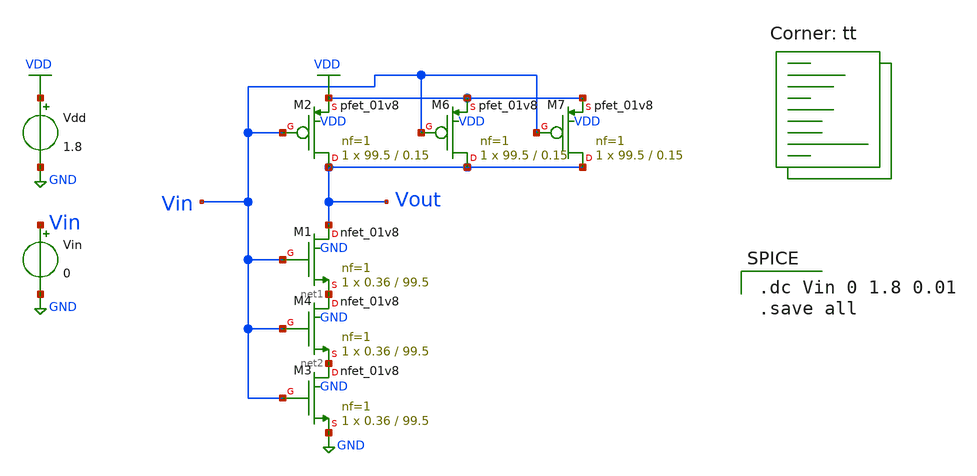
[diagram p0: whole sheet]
** sch_path: vdd1.8V/inverter_sat_16.sch
**.subckt inverter_sat_16
Vdd VDD GND 1.8
XM1 Vout Vin net1 GND sky130_fd_pr__nfet_01v8 L=99.5 W=0.36 nf=1 ad='int((nf+1)/2) * W/nf * 0.29' as='int((nf+2)/2) * W/nf * 0.29'
+ pd='2*int((nf+1)/2) * (W/nf + 0.29)' ps='2*int((nf+2)/2) * (W/nf + 0.29)' nrd='0.29 / W' nrs='0.29 / W'
+ sa=0 sb=0 sd=0 mult=1 m=1
XM2 Vout Vin VDD VDD sky130_fd_pr__pfet_01v8 L=0.15 W=99.5 nf=1 ad='int((nf+1)/2) * W/nf * 0.29' as='int((nf+2)/2) * W/nf * 0.29'
+ pd='2*int((nf+1)/2) * (W/nf + 0.29)' ps='2*int((nf+2)/2) * (W/nf + 0.29)' nrd='0.29 / W' nrs='0.29 / W'
+ sa=0 sb=0 sd=0 mult=1 m=1
Vin Vin GND 0
XM6 Vout Vin VDD VDD sky130_fd_pr__pfet_01v8 L=0.15 W=99.5 nf=1 ad='int((nf+1)/2) * W/nf * 0.29' as='int((nf+2)/2) * W/nf * 0.29'
+ pd='2*int((nf+1)/2) * (W/nf + 0.29)' ps='2*int((nf+2)/2) * (W/nf + 0.29)' nrd='0.29 / W' nrs='0.29 / W'
+ sa=0 sb=0 sd=0 mult=1 m=1
XM7 Vout Vin VDD VDD sky130_fd_pr__pfet_01v8 L=0.15 W=99.5 nf=1 ad='int((nf+1)/2) * W/nf * 0.29' as='int((nf+2)/2) * W/nf * 0.29'
+ pd='2*int((nf+1)/2) * (W/nf + 0.29)' ps='2*int((nf+2)/2) * (W/nf + 0.29)' nrd='0.29 / W' nrs='0.29 / W'
+ sa=0 sb=0 sd=0 mult=1 m=1
XM4 net1 Vin net2 GND sky130_fd_pr__nfet_01v8 L=99.5 W=0.36 nf=1 ad='int((nf+1)/2) * W/nf * 0.29' as='int((nf+2)/2) * W/nf * 0.29'
+ pd='2*int((nf+1)/2) * (W/nf + 0.29)' ps='2*int((nf+2)/2) * (W/nf + 0.29)' nrd='0.29 / W' nrs='0.29 / W'
+ sa=0 sb=0 sd=0 mult=1 m=1
XM3 net2 Vin GND GND sky130_fd_pr__nfet_01v8 L=99.5 W=0.36 nf=1 ad='int((nf+1)/2) * W/nf * 0.29' as='int((nf+2)/2) * W/nf * 0.29'
+ pd='2*int((nf+1)/2) * (W/nf + 0.29)' ps='2*int((nf+2)/2) * (W/nf + 0.29)' nrd='0.29 / W' nrs='0.29 / W'
+ sa=0 sb=0 sd=0 mult=1 m=1
**** begin user architecture code

.dc Vin 0 1.8 0.01
.save all

.lib $::SKYWATER_MODELS/sky130.lib.spice tt
**** end user architecture code
**.ends
.GLOBAL VDD
.GLOBAL GND
.end
